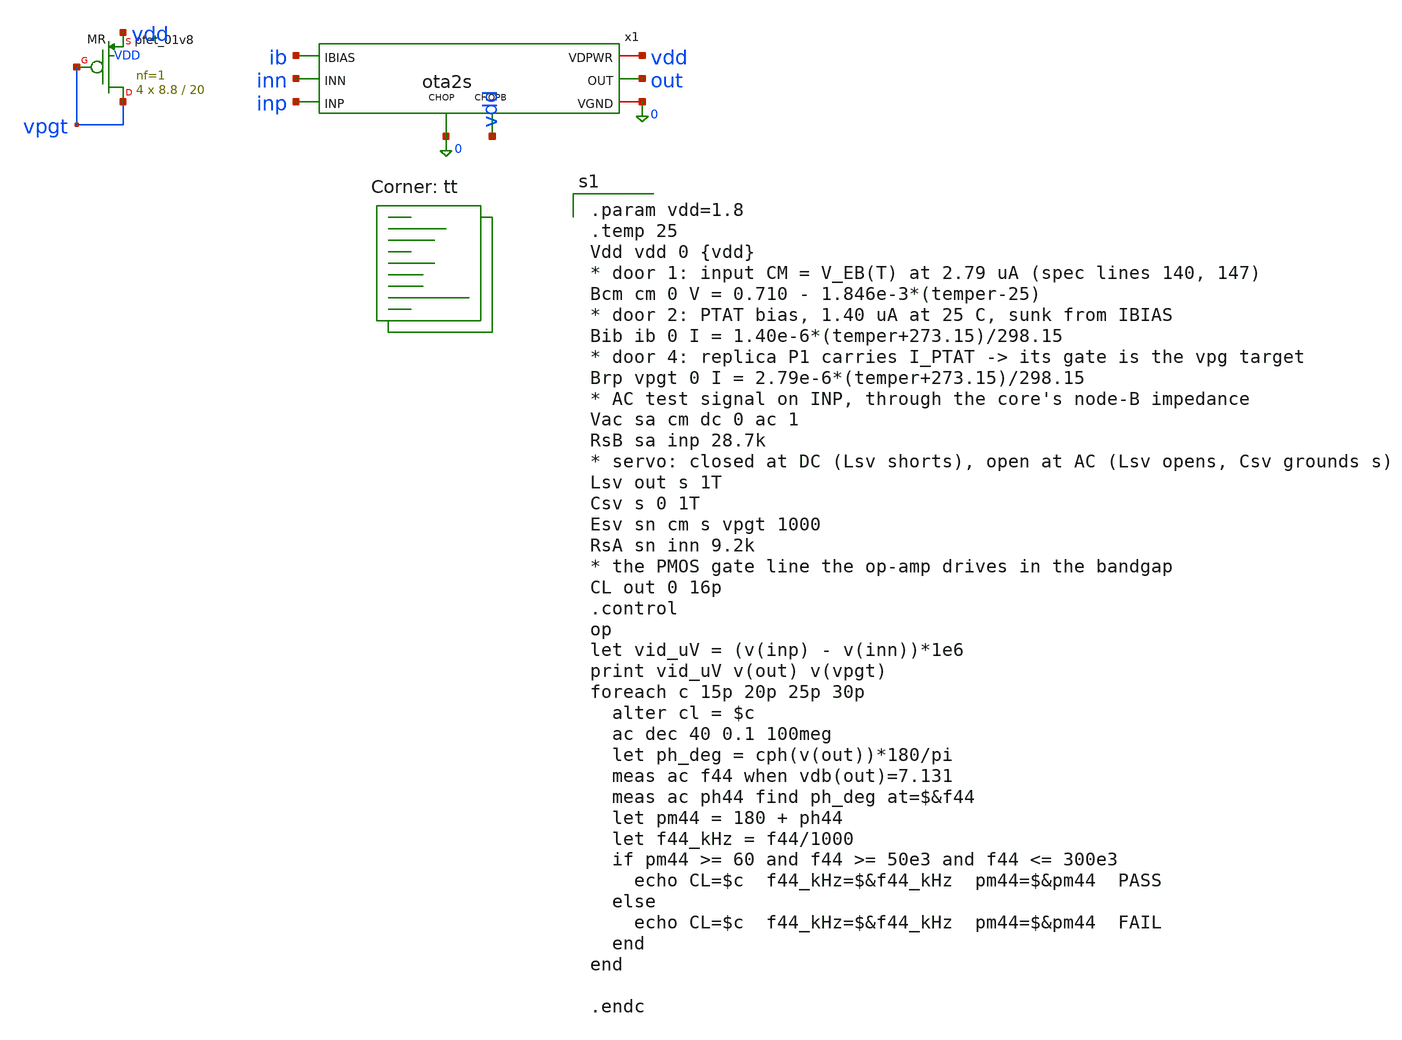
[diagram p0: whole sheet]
** sch_path: xschem/tb_ota2s_ol.sch
**.subckt tb_ota2s_ol
x1 inp inn out vdd 0 ib 0 vdd ota2s
XMR vpgt vpgt vdd VDD sky130_fd_pr__pfet_01v8 L=20 W=8.8 nf=1 ad='int((1 + 1)/2) * 8.8 / 1 * 0.29' as='int((1 + 2)/2) * 8.8 / 1 * 0.29'
+ pd='2*int((1 + 1)/2) * (8.8 / 1 + 0.29)' ps='2*int((1 + 2)/2) * (8.8 / 1 + 0.29)' nrd='0.29 / 8.8 ' nrs='0.29 / 8.8 '
+ sa=0 sb=0 sd=0 mult=4 m=4
**** begin user architecture code
.lib $::SKYWATER_MODELS/sky130.lib.spice tt

.param vdd=1.8
.temp 25
Vdd vdd 0 {vdd}
* door 1: input CM = V_EB(T) at 2.79 uA (spec lines 140, 147)
Bcm cm 0 V = 0.710 - 1.846e-3*(temper-25)
* door 2: PTAT bias, 1.40 uA at 25 C, sunk from IBIAS
Bib ib 0 I = 1.40e-6*(temper+273.15)/298.15
* door 4: replica P1 carries I_PTAT -> its gate is the vpg target
Brp vpgt 0 I = 2.79e-6*(temper+273.15)/298.15
* AC test signal on INP, through the core's node-B impedance
Vac sa cm dc 0 ac 1
RsB sa inp 28.7k
* servo: closed at DC (Lsv shorts), open at AC (Lsv opens, Csv grounds s)
Lsv out s 1T
Csv s 0 1T
Esv sn cm s vpgt 1000
RsA sn inn 9.2k
* the PMOS gate line the op-amp drives in the bandgap
CL out 0 16p
.control
op
let vid_uV = (v(inp) - v(inn))*1e6
print vid_uV v(out) v(vpgt)
foreach c 15p 20p 25p 30p
  alter cl = $c
  ac dec 40 0.1 100meg
  let ph_deg = cph(v(out))*180/pi
  meas ac f44 when vdb(out)=7.131
  meas ac ph44 find ph_deg at=$&f44
  let pm44 = 180 + ph44
  let f44_kHz = f44/1000
  if pm44 >= 60 and f44 >= 50e3 and f44 <= 300e3
    echo CL=$c  f44_kHz=$&f44_kHz  pm44=$&pm44  PASS
  else
    echo CL=$c  f44_kHz=$&f44_kHz  pm44=$&pm44  FAIL
  end
end

.endc

**** end user architecture code
**.ends

* expanding   symbol:  ota2s.sym # of pins=8
** sym_path: xschem/ota2s.sym
** sch_path: xschem/ota2s.sch
.subckt ota2s INP INN OUT VDPWR VGND IBIAS CHOP CHOPB
*.ipin INN
*.ipin INP
*.ipin IBIAS
*.opin OUT
*.iopin VDPWR
*.iopin VGND
*.ipin CHOPB
*.ipin CHOP
XMREF IBIAS IBIAS VDPWR VDPWR sky130_fd_pr__pfet_01v8 L=4 W=20 nf=1 ad='int((1 + 1)/2) * 20 / 1 * 0.29' as='int((1
+ + 2)/2) * 20 / 1 * 0.29' pd='2*int((1 + 1)/2) * (20 / 1 + 0.29)' ps='2*int((1 + 2)/2) * (20 / 1 + 0.29)' nrd='0.29
+ / 20 ' nrs='0.29 / 20 ' sa=0 sb=0 sd=0 mult=1 m=1
XMTAIL tail IBIAS VDPWR VDPWR sky130_fd_pr__pfet_01v8 L=4 W=20 nf=1 ad='int((1 + 1)/2) * 20 / 1 * 0.29' as='int((1
+ + 2)/2) * 20 / 1 * 0.29' pd='2*int((1 + 1)/2) * (20 / 1 + 0.29)' ps='2*int((1 + 2)/2) * (20 / 1 + 0.29)' nrd='0.29
+ / 20 ' nrs='0.29 / 20 ' sa=0 sb=0 sd=0 mult=2 m=2
XMP1 d1 INN tail VDPWR sky130_fd_pr__pfet_01v8_lvt L=6 W=25 nf=1 ad='int((1 + 1)/2) * 25 / 1 * 0.29' as='int((1
+ + 2)/2) * 25 / 1 * 0.29' pd='2*int((1 + 1)/2) * (25 / 1 + 0.29)' ps='2*int((1 + 2)/2) * (25 / 1 + 0.29)' nrd='0.29
+ / 25 ' nrs='0.29 / 25 ' sa=0 sb=0 sd=0 mult=24 m=24
XMP2 x1 INP tail VDPWR sky130_fd_pr__pfet_01v8_lvt L=6 W=25 nf=1 ad='int((1 + 1)/2) * 25 / 1 * 0.29' as='int((1
+ + 2)/2) * 25 / 1 * 0.29' pd='2*int((1 + 1)/2) * (25 / 1 + 0.29)' ps='2*int((1 + 2)/2) * (25 / 1 + 0.29)' nrd='0.29
+ / 25 ' nrs='0.29 / 25 ' sa=0 sb=0 sd=0 mult=24 m=24
XMN1 d1 g12 VGND VGND sky130_fd_pr__nfet_01v8 L=20 W=6 nf=1 ad='int((1 + 1)/2) * 6 / 1 * 0.29' as='int((1
+ + 2)/2) * 6 / 1 * 0.29' pd='2*int((1 + 1)/2) * (6 / 1 + 0.29)' ps='2*int((1 + 2)/2) * (6 / 1 + 0.29)' nrd='0.29
+ / 6 ' nrs='0.29 / 6 ' sa=0 sb=0 sd=0 mult=2 m=2
XMN2 x1 g12 VGND VGND sky130_fd_pr__nfet_01v8 L=20 W=6 nf=1 ad='int((1 + 1)/2) * 6 / 1 * 0.29' as='int((1
+ + 2)/2) * 6 / 1 * 0.29' pd='2*int((1 + 1)/2) * (6 / 1 + 0.29)' ps='2*int((1 + 2)/2) * (6 / 1 + 0.29)' nrd='0.29
+ / 6 ' nrs='0.29 / 6 ' sa=0 sb=0 sd=0 mult=2 m=2
XMP3 OUT IBIAS VDPWR VDPWR sky130_fd_pr__pfet_01v8 L=4 W=20 nf=1 ad='int((1 + 1)/2) * 20 / 1 * 0.29' as='int((1
+ + 2)/2) * 20 / 1 * 0.29' pd='2*int((1 + 1)/2) * (20 / 1 + 0.29)' ps='2*int((1 + 2)/2) * (20 / 1 + 0.29)' nrd='0.29
+ / 20 ' nrs='0.29 / 20 ' sa=0 sb=0 sd=0 mult=6 m=6
XMN3 OUT g3 VGND VGND sky130_fd_pr__nfet_01v8 L=1 W=7 nf=1 ad='int((1 + 1)/2) * 7 / 1 * 0.29' as='int((1
+ + 2)/2) * 7 / 1 * 0.29' pd='2*int((1 + 1)/2) * (7 / 1 + 0.29)' ps='2*int((1 + 2)/2) * (7 / 1 + 0.29)' nrd='0.29
+ / 7 ' nrs='0.29 / 7 ' sa=0 sb=0 sd=0 mult=1 m=1
XRZ1 net1 g3 VGND sky130_fd_pr__res_high_po_1p41 L=20 mult=1 m=1
XRZ2 net2 net1 VGND sky130_fd_pr__res_high_po_1p41 L=20 mult=1 m=1
XRZ3 net3 net2 VGND sky130_fd_pr__res_high_po_1p41 L=20 mult=1 m=1
XRZ4 net4 net3 VGND sky130_fd_pr__res_high_po_1p41 L=20 mult=1 m=1
XRZ5 net5 net4 VGND sky130_fd_pr__res_high_po_1p41 L=20 mult=1 m=1
XRZ6 cz net5 VGND sky130_fd_pr__res_high_po_1p41 L=20 mult=1 m=1
XCC cz OUT sky130_fd_pr__cap_mim_m3_1 W=25 L=25 MF=8 m=8
XDP tail VDPWR tail VDPWR sky130_fd_pr__pfet_01v8_lvt L=6 W=25 nf=1 ad='int((1 + 1)/2) * 25 / 1 * 0.29' as='int((1
+ + 2)/2) * 25 / 1 * 0.29' pd='2*int((1 + 1)/2) * (25 / 1 + 0.29)' ps='2*int((1 + 2)/2) * (25 / 1 + 0.29)' nrd='0.29
+ / 25 ' nrs='0.29 / 25 ' sa=0 sb=0 sd=0 mult=8 m=8
XDNA d1 VGND VGND VGND sky130_fd_pr__nfet_01v8 L=20 W=6 nf=1 ad='int((1 + 1)/2) * 6 / 1 * 0.29' as='int((1
+ + 2)/2) * 6 / 1 * 0.29' pd='2*int((1 + 1)/2) * (6 / 1 + 0.29)' ps='2*int((1 + 2)/2) * (6 / 1 + 0.29)' nrd='0.29
+ / 6 ' nrs='0.29 / 6 ' sa=0 sb=0 sd=0 mult=2 m=2
XDNB x1 VGND VGND VGND sky130_fd_pr__nfet_01v8 L=20 W=6 nf=1 ad='int((1 + 1)/2) * 6 / 1 * 0.29' as='int((1
+ + 2)/2) * 6 / 1 * 0.29' pd='2*int((1 + 1)/2) * (6 / 1 + 0.29)' ps='2*int((1 + 2)/2) * (6 / 1 + 0.29)' nrd='0.29
+ / 6 ' nrs='0.29 / 6 ' sa=0 sb=0 sd=0 mult=2 m=2
XDB VDPWR VDPWR VDPWR VDPWR sky130_fd_pr__pfet_01v8 L=4 W=20 nf=1 ad='int((1 + 1)/2) * 20 / 1 * 0.29' as='int((1
+ + 2)/2) * 20 / 1 * 0.29' pd='2*int((1 + 1)/2) * (20 / 1 + 0.29)' ps='2*int((1 + 2)/2) * (20 / 1 + 0.29)' nrd='0.29
+ / 20 ' nrs='0.29 / 20 ' sa=0 sb=0 sd=0 mult=2 m=2
XRD1 VGND VGND VGND sky130_fd_pr__res_high_po_1p41 L=20 mult=1 m=1
XRD2 VGND VGND VGND sky130_fd_pr__res_high_po_1p41 L=20 mult=1 m=1
XSD1 d1 CHOPB g12 VGND sky130_fd_pr__nfet_01v8 L=0.5 W=6 nf=1 ad='int((1 + 1)/2) * 6 / 1 * 0.29' as='int((1
+ + 2)/2) * 6 / 1 * 0.29' pd='2*int((1 + 1)/2) * (6 / 1 + 0.29)' ps='2*int((1 + 2)/2) * (6 / 1 + 0.29)' nrd='0.29
+ / 6 ' nrs='0.29 / 6 ' sa=0 sb=0 sd=0 mult=1 m=1
XSD2 x1 CHOP g12 VGND sky130_fd_pr__nfet_01v8 L=0.5 W=6 nf=1 ad='int((1 + 1)/2) * 6 / 1 * 0.29' as='int((1
+ + 2)/2) * 6 / 1 * 0.29' pd='2*int((1 + 1)/2) * (6 / 1 + 0.29)' ps='2*int((1 + 2)/2) * (6 / 1 + 0.29)' nrd='0.29
+ / 6 ' nrs='0.29 / 6 ' sa=0 sb=0 sd=0 mult=1 m=1
XSG2 g3 CHOP d1 VGND sky130_fd_pr__nfet_01v8 L=0.5 W=6 nf=1 ad='int((1 + 1)/2) * 6 / 1 * 0.29' as='int((1
+ + 2)/2) * 6 / 1 * 0.29' pd='2*int((1 + 1)/2) * (6 / 1 + 0.29)' ps='2*int((1 + 2)/2) * (6 / 1 + 0.29)' nrd='0.29
+ / 6 ' nrs='0.29 / 6 ' sa=0 sb=0 sd=0 mult=1 m=1
XSG1 x1 CHOPB g3 VGND sky130_fd_pr__nfet_01v8 L=0.5 W=6 nf=1 ad='int((1 + 1)/2) * 6 / 1 * 0.29' as='int((1
+ + 2)/2) * 6 / 1 * 0.29' pd='2*int((1 + 1)/2) * (6 / 1 + 0.29)' ps='2*int((1 + 2)/2) * (6 / 1 + 0.29)' nrd='0.29
+ / 6 ' nrs='0.29 / 6 ' sa=0 sb=0 sd=0 mult=1 m=1
.ends

.end
